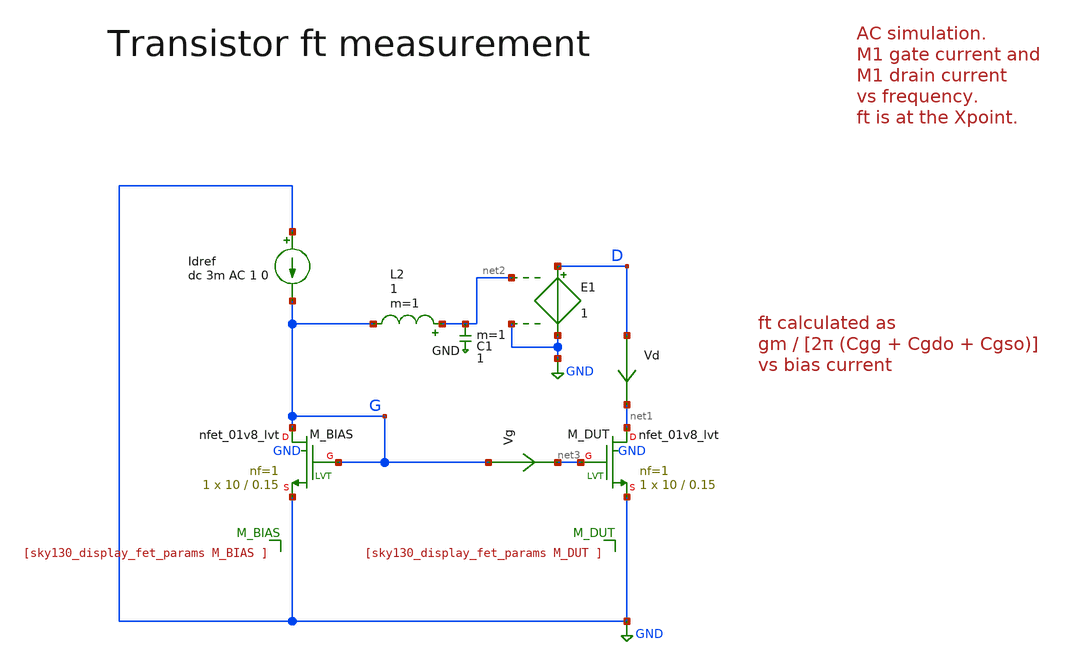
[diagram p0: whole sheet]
** sch_path: sky130A/xschem_libs/sky130_tests/tb_ft_test/schematic/tb_ft_test.sch
* Copyright 2021 Stefan Frederik Schippers
* Licensed under the Apache License, Version 2.0 (the "License");
* you may not use this file except in compliance with the License.
* You may obtain a copy of the License at
* https://www.apache.org/licenses/LICENSE-2.0
* Unless required by applicable law or agreed to in writing, software
* distributed under the License is distributed on an "AS IS" BASIS,
* WITHOUT WARRANTIES OR CONDITIONS OF ANY KIND, either express or implied.
* See the License for the specific language governing permissions and
* limitations under the License.
**.subckt tb_ft_test
XM_DUT net1 net3 GND GND sky130_fd_pr__nfet_01v8_lvt L=0.15 W=10 nf=1 ad='int((1 + 1)/2) * 10 / 1 * 0.29'
+ as='int((1 + 2)/2) * 10 / 1 * 0.29' pd='2*int((1 + 1)/2) * (10 / 1 + 0.29)' ps='2*int((1 + 2)/2) * (10 / 1 + 0.29)'
+ nrd='0.29 / 10 ' nrs='0.29 / 10 ' sa=0 sb=0 sd=0 mult=1 m=1
Idref GND G dc 3m AC 1 0
Vd D net1 0
.save i(vd)
Vg G net3 0
.save i(vg)
XM_BIAS G G GND GND sky130_fd_pr__nfet_01v8_lvt L=0.15 W=10 nf=1 ad='int((1 + 1)/2) * 10 / 1 * 0.29'
+ as='int((1 + 2)/2) * 10 / 1 * 0.29' pd='2*int((1 + 1)/2) * (10 / 1 + 0.29)' ps='2*int((1 + 2)/2) * (10 / 1 + 0.29)'
+ nrd='0.29 / 10 ' nrs='0.29 / 10 ' sa=0 sb=0 sd=0 mult=1 m=1
L2 net2 G 1 m=1
C1 net2 GND 1 m=1
E1 D GND net2 GND 1
**** begin user architecture code


.include tb_ft_test.save
* .options filetype=ascii
.option savecurrents
.save all
.control
*dc Idref 0.1e-3 10e-3 0.1e-3
let n_idx = 59
let start_iref = 0.1e-3
let stop_iref = 6e-3
let delta_iref = (stop_iref - start_iref) / n_idx
let iref_act = start_iref
let idx = 0
*loop
while iref_act le stop_iref
  alter idref iref_act
  op
  let gm = @m.xm_dut.msky130_fd_pr__nfet_01v8_lvt[gm]
  let ids = @m.xm_dut.msky130_fd_pr__nfet_01v8_lvt[id]
  let cgg =  @m.xm_dut.msky130_fd_pr__nfet_01v8_lvt[cgg]
  let cgso =  @m.xm_dut.msky130_fd_pr__nfet_01v8_lvt[cgso]
  let cgdo =  @m.xm_dut.msky130_fd_pr__nfet_01v8_lvt[cgdo]
  let ft = gm/(2*pi*(cgg + cgso + cgdo))

  setscale iref_act
  settype current iref_act
  write tb_ft_test.raw
  set appendwrite

  let iref_act = iref_act + delta_iref
  let idx = idx + 1
end

ac dec 10 1k 100G
remzerovec
write tb_ft_test.raw

.endc
.end



** opencircuitdesign pdks install
.lib $::SKYWATER_MODELS/sky130.lib.spice tt

**** end user architecture code
**.ends
.GLOBAL GND
.end
